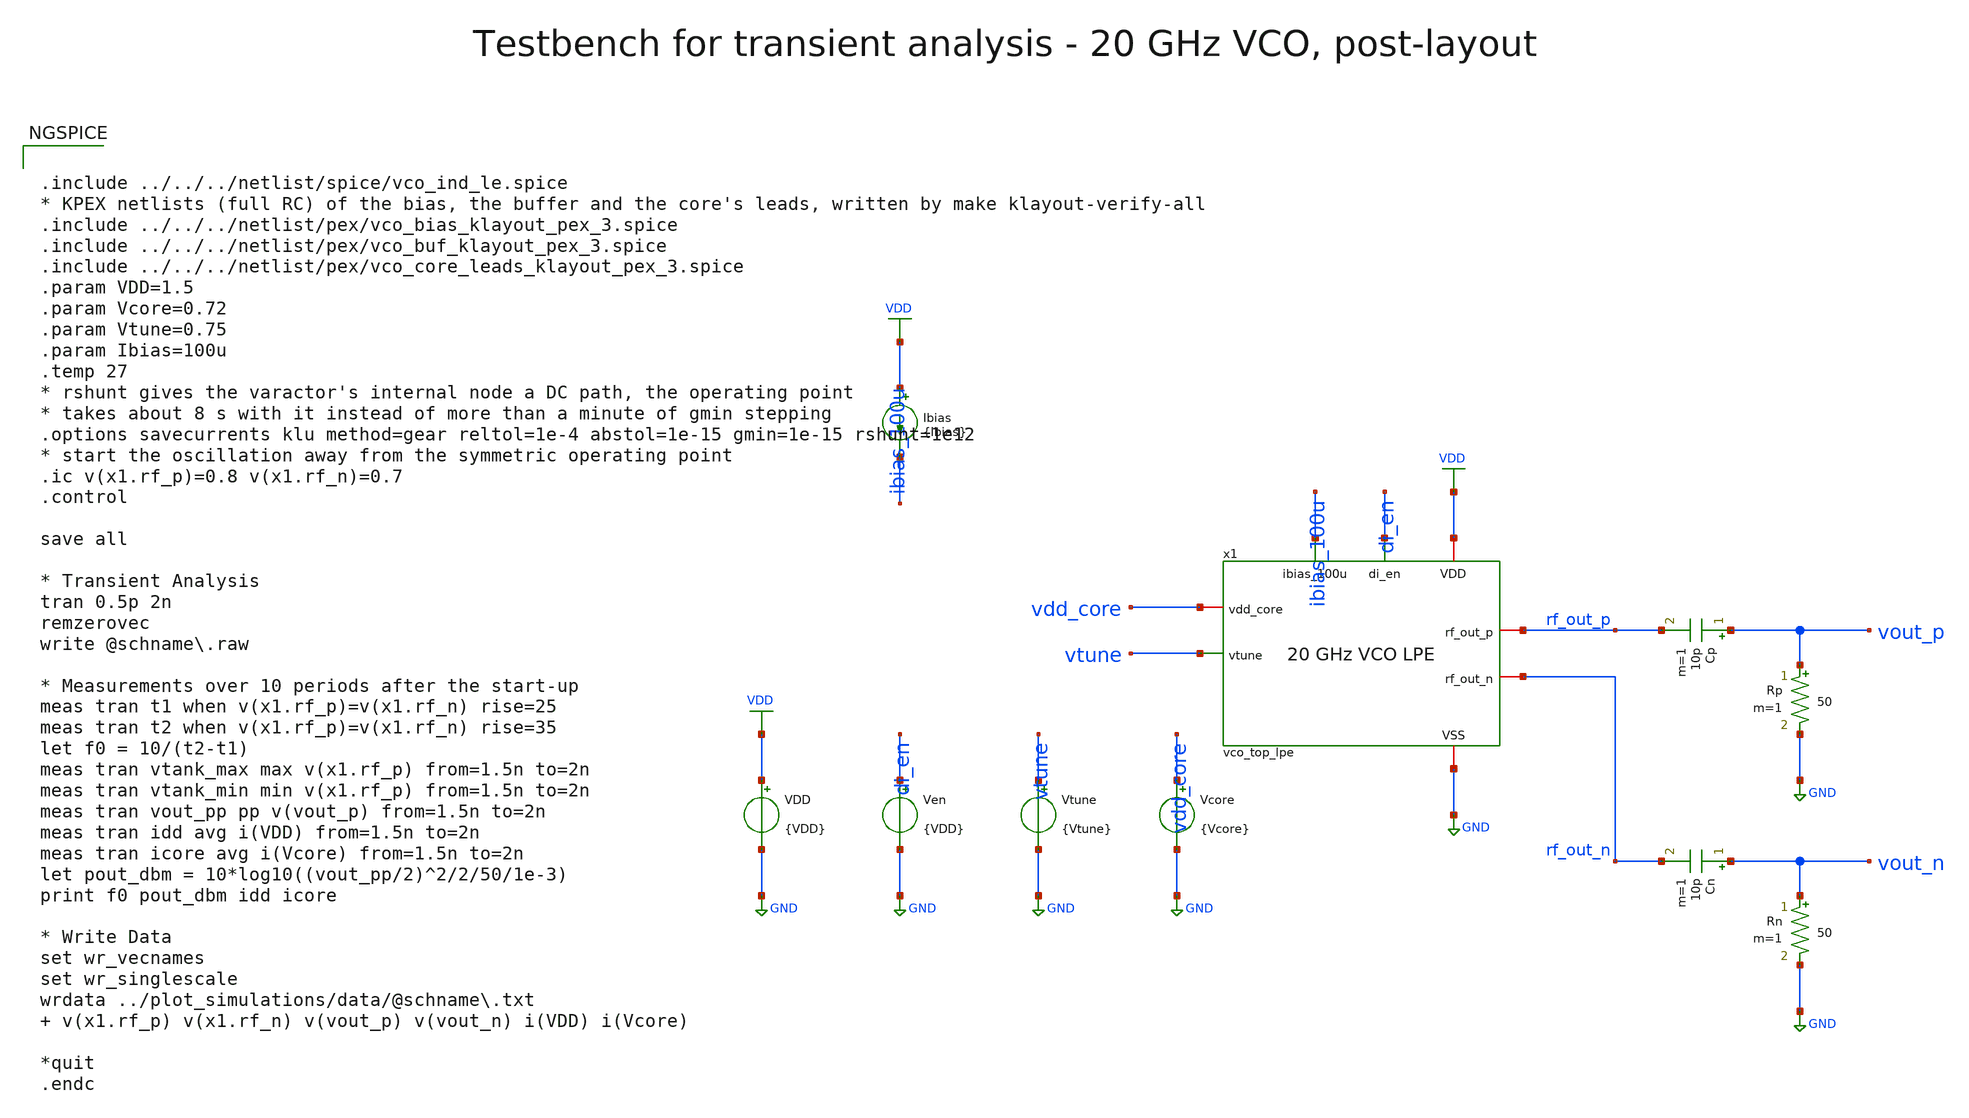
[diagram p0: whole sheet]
** sch_path: macros/vco/testbenches/xschem/vco_top_tb_tran_lpe.sch
**.subckt vco_top_tb_tran_lpe
x1 ibias_100u di_en VDD GND vdd_core vtune rf_out_p rf_out_n vco_top_lpe
Vcore vdd_core GND {Vcore}
Cp vout_p rf_out_p 10p m=1
Rp vout_p GND 50 m=1
Cn vout_n rf_out_n 10p m=1
Rn vout_n GND 50 m=1
VDD VDD GND {VDD}
Ven di_en GND {VDD}
Vtune vtune GND {Vtune}
Ibias VDD ibias_100u {Ibias}
**** begin user architecture code


.include ../../../netlist/spice/vco_ind_le.spice
* KPEX netlists (full RC) of the bias, the buffer and the core's leads, written by make klayout-verify-all
.include ../../../netlist/pex/vco_bias_klayout_pex_3.spice
.include ../../../netlist/pex/vco_buf_klayout_pex_3.spice
.include ../../../netlist/pex/vco_core_leads_klayout_pex_3.spice
.param VDD=1.5
.param Vcore=0.72
.param Vtune=0.75
.param Ibias=100u
.temp 27
* rshunt gives the varactor's internal node a DC path, the operating point
* takes about 8 s with it instead of more than a minute of gmin stepping
.options savecurrents klu method=gear reltol=1e-4 abstol=1e-15 gmin=1e-15 rshunt=1e12
* start the oscillation away from the symmetric operating point
.ic v(x1.rf_p)=0.8 v(x1.rf_n)=0.7
.control

save all

* Transient Analysis
tran 0.5p 2n
remzerovec
write @schname\.raw

* Measurements over 10 periods after the start-up
meas tran t1 when v(x1.rf_p)=v(x1.rf_n) rise=25
meas tran t2 when v(x1.rf_p)=v(x1.rf_n) rise=35
let f0 = 10/(t2-t1)
meas tran vtank_max max v(x1.rf_p) from=1.5n to=2n
meas tran vtank_min min v(x1.rf_p) from=1.5n to=2n
meas tran vout_pp pp v(vout_p) from=1.5n to=2n
meas tran idd avg i(VDD) from=1.5n to=2n
meas tran icore avg i(Vcore) from=1.5n to=2n
let pout_dbm = 10*log10((vout_pp/2)^2/2/50/1e-3)
print f0 pout_dbm idd icore

* Write Data
set wr_vecnames
set wr_singlescale
wrdata ../plot_simulations/data/@schname\.txt  v(x1.rf_p) v(x1.rf_n) v(vout_p) v(vout_n) i(VDD)
+ i(Vcore)

*quit
.endc



.lib cornerMOSlv.lib mos_tt
.lib cornerMOShv.lib mos_tt
.lib cornerRES.lib res_typ
.lib cornerCAP.lib cap_typ

**** end user architecture code
**.ends

* expanding   symbol:  vco_top_lpe.sym # of pins=8
** sym_path: macros/vco/testbenches/xschem/vco_top_lpe.sym
** sch_path: macros/vco/testbenches/xschem/vco_top_lpe.sch
.subckt vco_top_lpe ibias_100u di_en VDD VSS vdd_core vtune rf_out_p rf_out_n
*.iopin VDD
*.iopin VSS
*.iopin vdd_core
*.ipin ibias_100u
*.ipin di_en
*.ipin vtune
*.iopin rf_out_p
*.iopin rf_out_n
xbias ibias_100u di_en VDD VSS vbg_buf vbn_buf vco_bias_pex
xcore vdd_core VSS vtune rf_p rf_n vco_core_lpe
xbuf vbn_buf vbg_buf VDD VSS rf_p rf_n rf_out_p rf_out_n vco_buf_pex
.ends


* expanding   symbol:  vco_core_lpe.sym # of pins=5
** sym_path: macros/vco/testbenches/xschem/vco_core_lpe.sym
** sch_path: macros/vco/testbenches/xschem/vco_core_lpe.sch
.subckt vco_core_lpe vdd_core VSS vtune rf_p rf_n
*.iopin vdd_core
*.iopin VSS
*.ipin vtune
*.iopin rf_p
*.iopin rf_n
xleads vdd_core VSS vtune rf_p rf_n vco_core_leads
xind rf_p rf_n vdd_core VSS vco_ind
xvar rf_p rf_n vtune VSS vco_var
.ends


* expanding   symbol:  vco_ind.sym # of pins=4
** sym_path: macros/vco/schematic/xschem/vco_ind.sym
** sch_path: macros/vco/schematic/xschem/vco_ind.sch
.subckt vco_ind la lb lc VSS
*.iopin la
*.iopin lc
*.iopin lb
*.iopin VSS
XL1 la lc lb VSS inductor3 w=4e-6 s=4e-6 d=52e-6 nr_r=2 m=1
x1 la lb lc vco_ind_le
.ends


* expanding   symbol:  vco_var.sym # of pins=4
** sym_path: macros/vco/schematic/xschem/vco_var.sym
** sch_path: macros/vco/schematic/xschem/vco_var.sch
.subckt vco_var rf_p rf_n vtune VSS
*.ipin vtune
*.iopin rf_p
*.iopin rf_n
*.iopin VSS
XCvar1 rf_p vtune rf_n VSS sg13_hv_svaricap w=3.74u l=0.3u Nx=7 mm_ok=1
XCvar2 rf_p vtune rf_n VSS sg13_hv_svaricap w=3.74u l=0.3u Nx=7 mm_ok=1
XCvar3 rf_p vtune rf_n VSS sg13_hv_svaricap w=3.74u l=0.3u Nx=7 mm_ok=1
.ends

.GLOBAL VDD
.GLOBAL GND
.end
